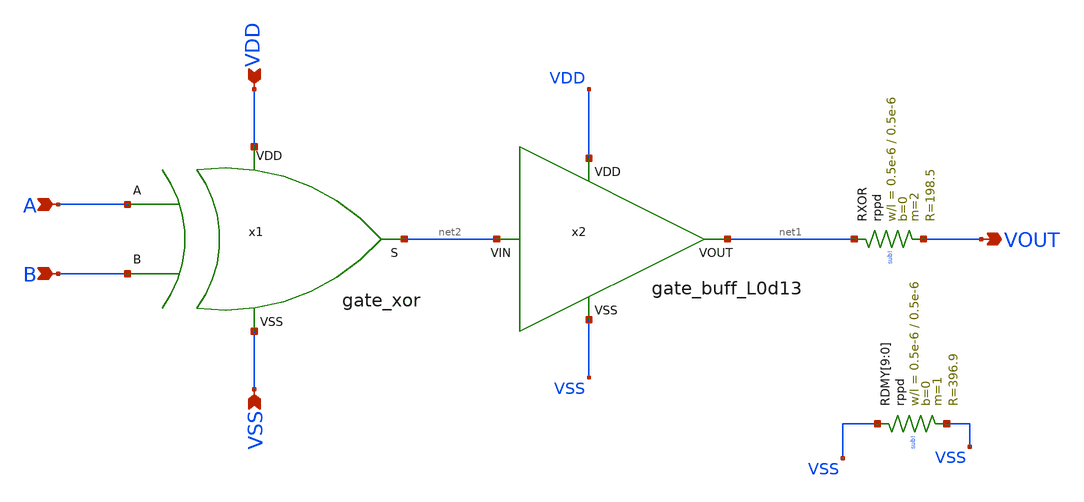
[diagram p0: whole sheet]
** sch_path: work/integrator_phasedetector/xschem/integrator_phasedetector.sch
**.subckt integrator_phasedetector A B VSS VDD VOUT
*.ipin A
*.ipin B
*.ipin VSS
*.ipin VDD
*.opin VOUT
x1 VDD net2 B A VSS gate_xor
x2 VDD net2 net1 VSS gate_buff_L0d13
XRXOR net1 VOUT sub! rppd w=0.5e-6 l=0.5e-6 m=2 b=0 mm_ok=1
XRDMY[9] VSS VSS sub! rppd w=0.5e-6 l=0.5e-6 m=1 b=0 mm_ok=1
XRDMY[8] VSS VSS sub! rppd w=0.5e-6 l=0.5e-6 m=1 b=0 mm_ok=1
XRDMY[7] VSS VSS sub! rppd w=0.5e-6 l=0.5e-6 m=1 b=0 mm_ok=1
XRDMY[6] VSS VSS sub! rppd w=0.5e-6 l=0.5e-6 m=1 b=0 mm_ok=1
XRDMY[5] VSS VSS sub! rppd w=0.5e-6 l=0.5e-6 m=1 b=0 mm_ok=1
XRDMY[4] VSS VSS sub! rppd w=0.5e-6 l=0.5e-6 m=1 b=0 mm_ok=1
XRDMY[3] VSS VSS sub! rppd w=0.5e-6 l=0.5e-6 m=1 b=0 mm_ok=1
XRDMY[2] VSS VSS sub! rppd w=0.5e-6 l=0.5e-6 m=1 b=0 mm_ok=1
XRDMY[1] VSS VSS sub! rppd w=0.5e-6 l=0.5e-6 m=1 b=0 mm_ok=1
XRDMY[0] VSS VSS sub! rppd w=0.5e-6 l=0.5e-6 m=1 b=0 mm_ok=1
**.ends
.end
